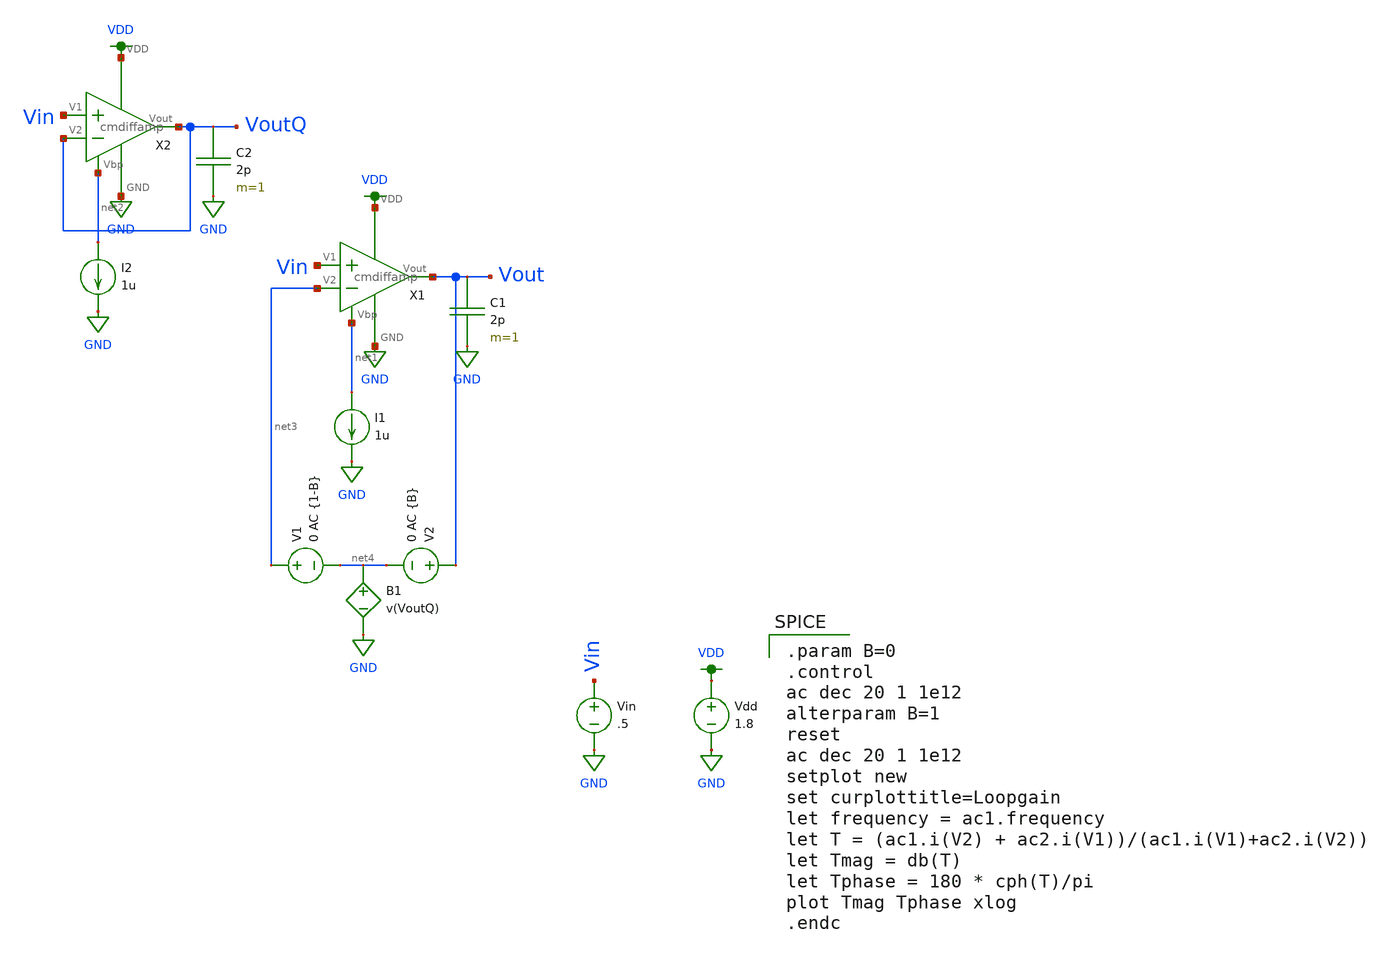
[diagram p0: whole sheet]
** sch_path: Miniproject3/SImulations/loopgain_sim.sch
**.subckt loopgain_sim
Vin Vin GND .5
Vdd VDD GND 1.8
I1 net1 GND 1u
C1 Vout GND 2p m=1
X1 Vout GND VDD Vin net3 net1 cmdiffamp
I2 net2 GND 1u
C2 VoutQ GND 2p m=1
X2 VoutQ GND VDD Vin VoutQ net2 cmdiffamp
V1 net3 net4 0 AC {1-B}
V2 Vout net4 0 AC {B}
B1 net4 GND V=v(VoutQ)
**** begin user architecture code

.option wnflag=1
.lib ~/skywater/skywater-pdk/libraries/sky130_fd_pr_ngspice/latest/models/sky130.lib.spice tt


.param B=0
.control
ac dec 20 1 1e12
alterparam B=1
reset
ac dec 20 1 1e12
setplot new
set curplottitle=Loopgain
let frequency = ac1.frequency
let T = (ac1.i(V2) + ac2.i(V1))/(ac1.i(V1)+ac2.i(V2))
let Tmag = db(T)
let Tphase = 180 * cph(T)/pi
plot Tmag Tphase xlog
.endc

**** end user architecture code
**.ends
.GLOBAL VDD
.GLOBAL GND
.end
